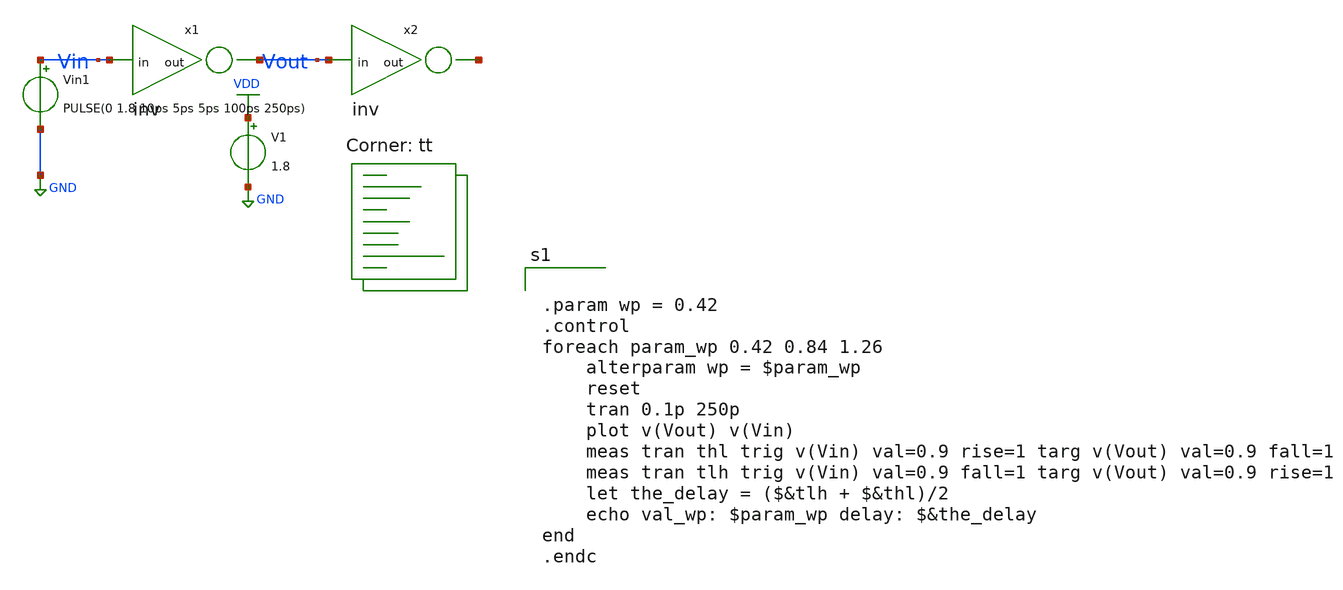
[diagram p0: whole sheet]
** sch_path: tut3/expt1_a/expt1_a.sch
**.subckt expt1_a
Vin1 Vin GND PULSE(0 1.8 10ps 5ps 5ps 100ps 250ps)
V1 VDD GND 1.8
x1 Vout Vin inv
x2 net1 Vout inv
**** begin user architecture code
.lib $::SKYWATER_MODELS/sky130.lib.spice tt


.param wp = 0.42
.control
foreach param_wp 0.42 0.84 1.26
	alterparam wp = $param_wp
	reset
	tran 0.1p 250p
	plot v(Vout) v(Vin)
	meas tran thl trig v(Vin) val=0.9 rise=1 targ v(Vout) val=0.9 fall=1
	meas tran tlh trig v(Vin) val=0.9 fall=1 targ v(Vout) val=0.9 rise=1
	let the_delay = ($&tlh + $&thl)/2
	echo val_wp: $param_wp delay: $&the_delay
end
.endc


**** end user architecture code
**.ends

* expanding   symbol:  /home/ee24s053/ee5311-2025/tut3/syms/inv.sym # of pins=2
** sym_path: tut3/syms/inv.sym
** sch_path: tut3/syms/inv.sch
.subckt inv out in
*.ipin in
*.opin out
XM1 out in VDD VDD sky130_fd_pr__pfet_01v8 L=0.15 W={wp} nf=1 ad='int((nf+1)/2) * W/nf * 0.29' as='int((nf+2)/2) * W/nf * 0.29'
+ pd='2*int((nf+1)/2) * (W/nf + 0.29)' ps='2*int((nf+2)/2) * (W/nf + 0.29)' nrd='0.29 / W' nrs='0.29 / W'
+ sa=0 sb=0 sd=0 mult=1 m=1
XM2 out in GND GND sky130_fd_pr__nfet_01v8 L=0.15 W=1 nf=1 ad='int((nf+1)/2) * W/nf * 0.29' as='int((nf+2)/2) * W/nf * 0.29'
+ pd='2*int((nf+1)/2) * (W/nf + 0.29)' ps='2*int((nf+2)/2) * (W/nf + 0.29)' nrd='0.29 / W' nrs='0.29 / W'
+ sa=0 sb=0 sd=0 mult=1 m=1
.ends

.GLOBAL GND
.GLOBAL VDD
.end
